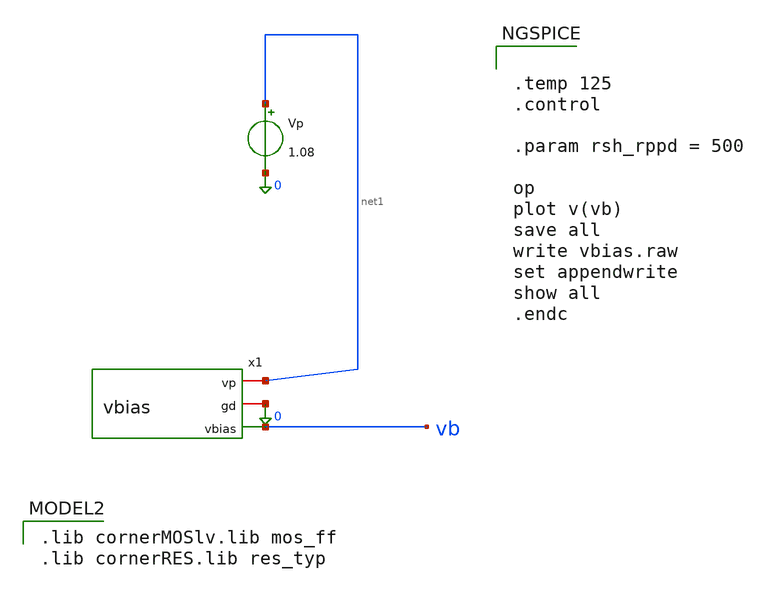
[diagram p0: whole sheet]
** sch_path: PLL0663-main/testbenches/tran/xschem/charge_pump/vbias_tb.sch
**.subckt vbias_tb
Vp net1 0 1.08
x1 net1 0 vb vbias
**** begin user architecture code


.temp 125
.control

.param rsh_rppd = 500

op
plot v(vb)
save all
write vbias.raw
set appendwrite
show all
.endc


 .lib cornerMOSlv.lib mos_ff
.lib cornerRES.lib res_typ




**** end user architecture code
**.ends

* expanding   symbol:
*+  /foss/designs/IHP__PLL0663/PLL0663-main/schematic/xschem/charge_pump/vbias.sym # of pins=3
** sym_path: /foss/designs/IHP__PLL0663/PLL0663-main/schematic/xschem/charge_pump/vbias.sym
** sch_path: /foss/designs/IHP__PLL0663/PLL0663-main/schematic/xschem/charge_pump/vbias.sch
.subckt vbias vp gd vbias
*.opin vbias
*.iopin gd
*.iopin vp
XM5 net1 iref vp vp sg13_lv_pmos w=1.2u l=0.6u ng=1 m=1 mm_ok=1
XM6 vbias net1 net2 gd sg13_lv_nmos w=3.6u l=0.6u ng=1 m=1 mm_ok=1
XM2 net2 net2 gd gd sg13_lv_nmos w=1.2u l=0.6u ng=1 m=1 mm_ok=1
XM3 gd gd gd gd sg13_lv_nmos w=1.86u l=0.6u ng=1 m=1 mm_ok=1
XM7 vp vp vp vp sg13_lv_pmos w=1.375u l=0.6u ng=1 m=1 mm_ok=1
XR1 net1 vbias gd rppd w=1e-6 l=1.7e-6 m=1 b=0 mm_ok=1
x1 vp iref gd curr_source
.ends


* expanding   symbol:
*+  /foss/designs/IHP__PLL0663/PLL0663-main/schematic/xschem/charge_pump/curr_source.sym # of pins=3
** sym_path: /foss/designs/IHP__PLL0663/PLL0663-main/schematic/xschem/charge_pump/curr_source.sym
** sch_path: /foss/designs/IHP__PLL0663/PLL0663-main/schematic/xschem/charge_pump/curr_source.sch
.subckt curr_source vp iref gd
*.iopin vp
*.iopin gd
*.opin iref
XM9 net3 net3 gd gd sg13_lv_nmos w=1u l=0.6u ng=1 m=1 mm_ok=1
XM4 iref iref vp vp sg13_lv_pmos w=1.4u l=0.6u ng=1 m=1 mm_ok=1
XM5 net2 iref vp vp sg13_lv_pmos w=1.2u l=0.6u ng=1 m=1 mm_ok=1
XM10 iref net2 net1 gd sg13_lv_nmos w=1.2u l=0.6u ng=1 m=1 mm_ok=1
XM1 net2 net2 gd gd sg13_lv_nmos w=1.4u l=0.6u ng=1 m=1 mm_ok=1
XM3 vp vp net3 gd sg13_lv_nmos w=1u l=0.6u ng=1 m=1 mm_ok=1
XM6 vp net3 iref gd sg13_lv_nmos w=1u l=0.6u ng=1 m=1 mm_ok=1
XM2 gd gd gd gd sg13_lv_nmos w=0.4u l=0.6u ng=1 m=1 mm_ok=1
XR2 net1 gd gd rppd w=1e-6 l=1.7e-6 m=1 b=0 mm_ok=1
.ends

.end
